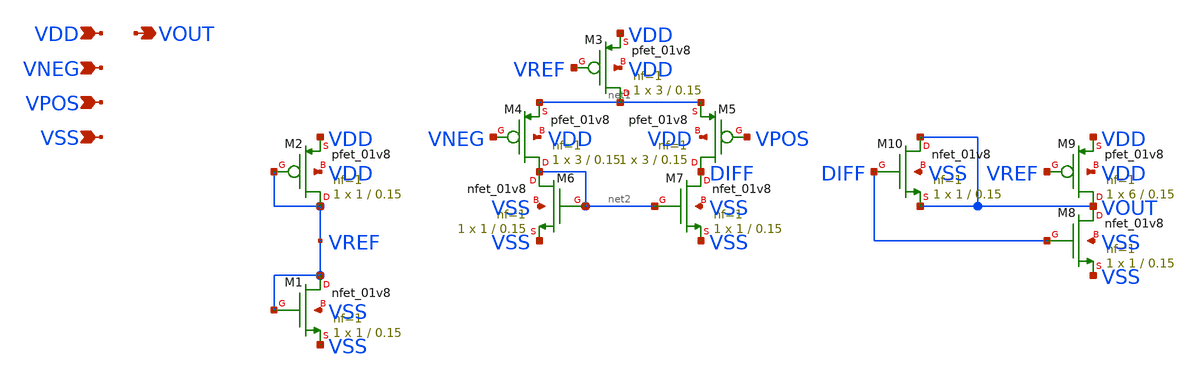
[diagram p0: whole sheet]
** sch_path: week4/xschem/adc/adc.sch
**.subckt adc VDD VOUT VSS VNEG VPOS
*.ipin VDD
*.opin VOUT
*.ipin VSS
*.ipin VNEG
*.ipin VPOS
XM1 VREF VREF VSS VSS sky130_fd_pr__nfet_01v8 L=0.15 W=1 nf=1 ad='int((nf+1)/2) * W/nf * 0.29' as='int((nf+2)/2) * W/nf * 0.29'
+ pd='2*int((nf+1)/2) * (W/nf + 0.29)' ps='2*int((nf+2)/2) * (W/nf + 0.29)' nrd='0.29 / W' nrs='0.29 / W'
+ sa=0 sb=0 sd=0 mult=1 m=1
XM2 VREF VREF VDD VDD sky130_fd_pr__pfet_01v8 L=0.15 W=1 nf=1 ad='int((nf+1)/2) * W/nf * 0.29' as='int((nf+2)/2) * W/nf * 0.29'
+ pd='2*int((nf+1)/2) * (W/nf + 0.29)' ps='2*int((nf+2)/2) * (W/nf + 0.29)' nrd='0.29 / W' nrs='0.29 / W'
+ sa=0 sb=0 sd=0 mult=1 m=1
XM3 net1 VREF VDD VDD sky130_fd_pr__pfet_01v8 L=0.15 W=3 nf=1 ad='int((nf+1)/2) * W/nf * 0.29' as='int((nf+2)/2) * W/nf * 0.29'
+ pd='2*int((nf+1)/2) * (W/nf + 0.29)' ps='2*int((nf+2)/2) * (W/nf + 0.29)' nrd='0.29 / W' nrs='0.29 / W'
+ sa=0 sb=0 sd=0 mult=1 m=1
XM4 net2 VNEG net1 VDD sky130_fd_pr__pfet_01v8 L=0.15 W=3 nf=1 ad='int((nf+1)/2) * W/nf * 0.29' as='int((nf+2)/2) * W/nf * 0.29'
+ pd='2*int((nf+1)/2) * (W/nf + 0.29)' ps='2*int((nf+2)/2) * (W/nf + 0.29)' nrd='0.29 / W' nrs='0.29 / W'
+ sa=0 sb=0 sd=0 mult=1 m=1
XM5 DIFF VPOS net1 VDD sky130_fd_pr__pfet_01v8 L=0.15 W=3 nf=1 ad='int((nf+1)/2) * W/nf * 0.29' as='int((nf+2)/2) * W/nf * 0.29'
+ pd='2*int((nf+1)/2) * (W/nf + 0.29)' ps='2*int((nf+2)/2) * (W/nf + 0.29)' nrd='0.29 / W' nrs='0.29 / W'
+ sa=0 sb=0 sd=0 mult=1 m=1
XM6 net2 net2 VSS VSS sky130_fd_pr__nfet_01v8 L=0.15 W=1 nf=1 ad='int((nf+1)/2) * W/nf * 0.29' as='int((nf+2)/2) * W/nf * 0.29'
+ pd='2*int((nf+1)/2) * (W/nf + 0.29)' ps='2*int((nf+2)/2) * (W/nf + 0.29)' nrd='0.29 / W' nrs='0.29 / W'
+ sa=0 sb=0 sd=0 mult=1 m=1
XM7 DIFF net2 VSS VSS sky130_fd_pr__nfet_01v8 L=0.15 W=1 nf=1 ad='int((nf+1)/2) * W/nf * 0.29' as='int((nf+2)/2) * W/nf * 0.29'
+ pd='2*int((nf+1)/2) * (W/nf + 0.29)' ps='2*int((nf+2)/2) * (W/nf + 0.29)' nrd='0.29 / W' nrs='0.29 / W'
+ sa=0 sb=0 sd=0 mult=1 m=1
XM8 VOUT DIFF VSS VSS sky130_fd_pr__nfet_01v8 L=0.15 W=1 nf=1 ad='int((nf+1)/2) * W/nf * 0.29' as='int((nf+2)/2) * W/nf * 0.29'
+ pd='2*int((nf+1)/2) * (W/nf + 0.29)' ps='2*int((nf+2)/2) * (W/nf + 0.29)' nrd='0.29 / W' nrs='0.29 / W'
+ sa=0 sb=0 sd=0 mult=1 m=1
XM9 VOUT VREF VDD VDD sky130_fd_pr__pfet_01v8 L=0.15 W=6 nf=1 ad='int((nf+1)/2) * W/nf * 0.29' as='int((nf+2)/2) * W/nf * 0.29'
+ pd='2*int((nf+1)/2) * (W/nf + 0.29)' ps='2*int((nf+2)/2) * (W/nf + 0.29)' nrd='0.29 / W' nrs='0.29 / W'
+ sa=0 sb=0 sd=0 mult=1 m=1
XM10 VOUT DIFF VOUT VSS sky130_fd_pr__nfet_01v8 L=0.15 W=1 nf=1 ad='int((nf+1)/2) * W/nf * 0.29' as='int((nf+2)/2) * W/nf * 0.29'
+ pd='2*int((nf+1)/2) * (W/nf + 0.29)' ps='2*int((nf+2)/2) * (W/nf + 0.29)' nrd='0.29 / W' nrs='0.29 / W'
+ sa=0 sb=0 sd=0 mult=1 m=1
**.ends
.end
